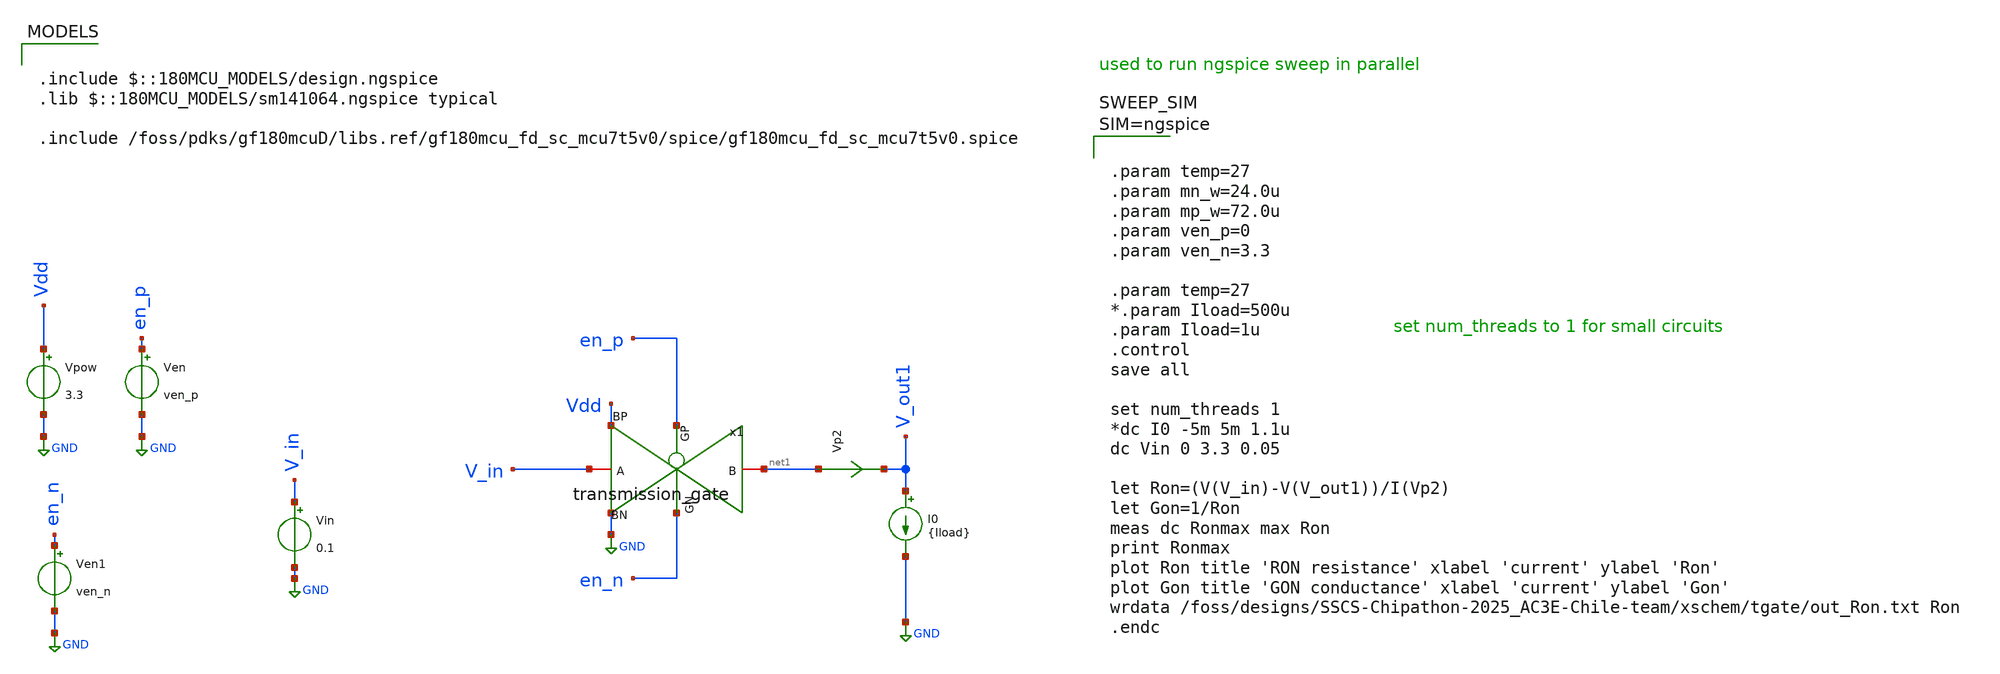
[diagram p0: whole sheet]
** sch_path: designs/switch_matrix_gf180mcu_9t5v0-main/tgate_PK/old/tgate_lv_vsweep_tb.sch
**.subckt tgate_lv_vsweep_tb
Vpow Vdd GND 3.3
Vin V_in GND 0.1
Ven en_p GND ven_p
Ven1 en_n GND ven_n
I0 V_out1 GND {Iload}
Vp2 net1 V_out1 0
.save i(vp2)
x1 net1 en_n en_p V_in Vdd GND transmission_gate
**** begin user architecture code



.param temp=27
.param mn_w=24.0u
.param mp_w=72.0u
.param ven_p=0
.param ven_n=3.3

.param temp=27
*.param Iload=500u
.param Iload=1u
.control
save all

set num_threads 1
*dc I0 -5m 5m 1.1u
dc Vin 0 3.3 0.05

let Ron=(V(V_in)-V(V_out1))/I(Vp2)
let Gon=1/Ron
meas dc Ronmax max Ron
print Ronmax
plot Ron title 'RON resistance' xlabel 'current' ylabel 'Ron'
plot Gon title 'GON conductance' xlabel 'current' ylabel 'Gon'
wrdata /foss/designs/SSCS-Chipathon-2025_AC3E-Chile-team/xschem/tgate/out_Ron.txt Ron
.endc




.include $::180MCU_MODELS/design.ngspice
.lib $::180MCU_MODELS/sm141064.ngspice typical

.include /foss/pdks/gf180mcuD/libs.ref/gf180mcu_fd_sc_mcu7t5v0/spice/gf180mcu_fd_sc_mcu7t5v0.spice

**** end user architecture code
**.ends

* expanding   symbol:  transmission_gate.sym # of pins=6
** sym_path: designs/switch_matrix_gf180mcu_9t5v0-main/tgate_PK/transmission_gate.sym
** sch_path: designs/switch_matrix_gf180mcu_9t5v0-main/tgate_PK/transmission_gate.sch
.subckt transmission_gate B GN GP A BP BN
*.iopin B
*.iopin GN
*.iopin A
*.iopin GP
*.iopin BN
*.iopin BP
XM1 A GN B BN nfet_03v3 L=0.28u W=mn_w nf=6 ad='int((nf+1)/2) * W/nf * 0.18u' as='int((nf+2)/2) * W/nf * 0.18u'
+ pd='2*int((nf+1)/2) * (W/nf + 0.18u)' ps='2*int((nf+2)/2) * (W/nf + 0.18u)' nrd='0.18u / W' nrs='0.18u / W'
+ sa=0 sb=0 sd=0 m=1
XM2 A GP B BP pfet_03v3 L=0.28u W=mp_w nf=6 ad='int((nf+1)/2) * W/nf * 0.18u' as='int((nf+2)/2) * W/nf * 0.18u'
+ pd='2*int((nf+1)/2) * (W/nf + 0.18u)' ps='2*int((nf+2)/2) * (W/nf + 0.18u)' nrd='0.18u / W' nrs='0.18u / W'
+ sa=0 sb=0 sd=0 m=1
.ends

.GLOBAL GND
.end
